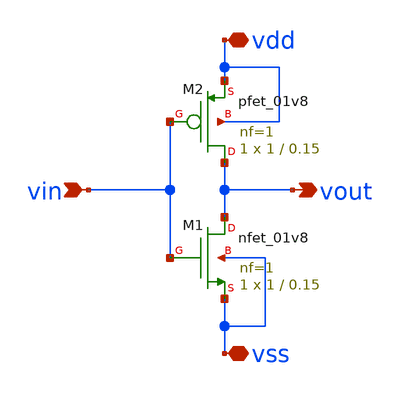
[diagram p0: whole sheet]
** sch_path: Lab1_inverter/xschem/inv.sch
**.subckt inv vin vout vdd vss
*.ipin vin
*.opin vout
*.iopin vdd
*.iopin vss
XM1 vout vin vss vss sky130_fd_pr__nfet_01v8 L=0.15 W=1 nf=1 ad='int((1 + 1)/2) * 1 / 1 * 0.29' as='int((1 + 2)/2) * 1 / 1 * 0.29'
+ pd='2*int((1 + 1)/2) * (1 / 1 + 0.29)' ps='2*int((1 + 2)/2) * (1 / 1 + 0.29)' nrd='0.29 / 1 ' nrs='0.29 / 1 '
+ sa=0 sb=0 sd=0 mult=1 m=1
XM2 vout vin vdd vdd sky130_fd_pr__pfet_01v8 L=0.15 W=1 nf=1 ad='int((1 + 1)/2) * 1 / 1 * 0.29' as='int((1 + 2)/2) * 1 / 1 * 0.29'
+ pd='2*int((1 + 1)/2) * (1 / 1 + 0.29)' ps='2*int((1 + 2)/2) * (1 / 1 + 0.29)' nrd='0.29 / 1 ' nrs='0.29 / 1 '
+ sa=0 sb=0 sd=0 mult=1 m=1
**.ends
.end
